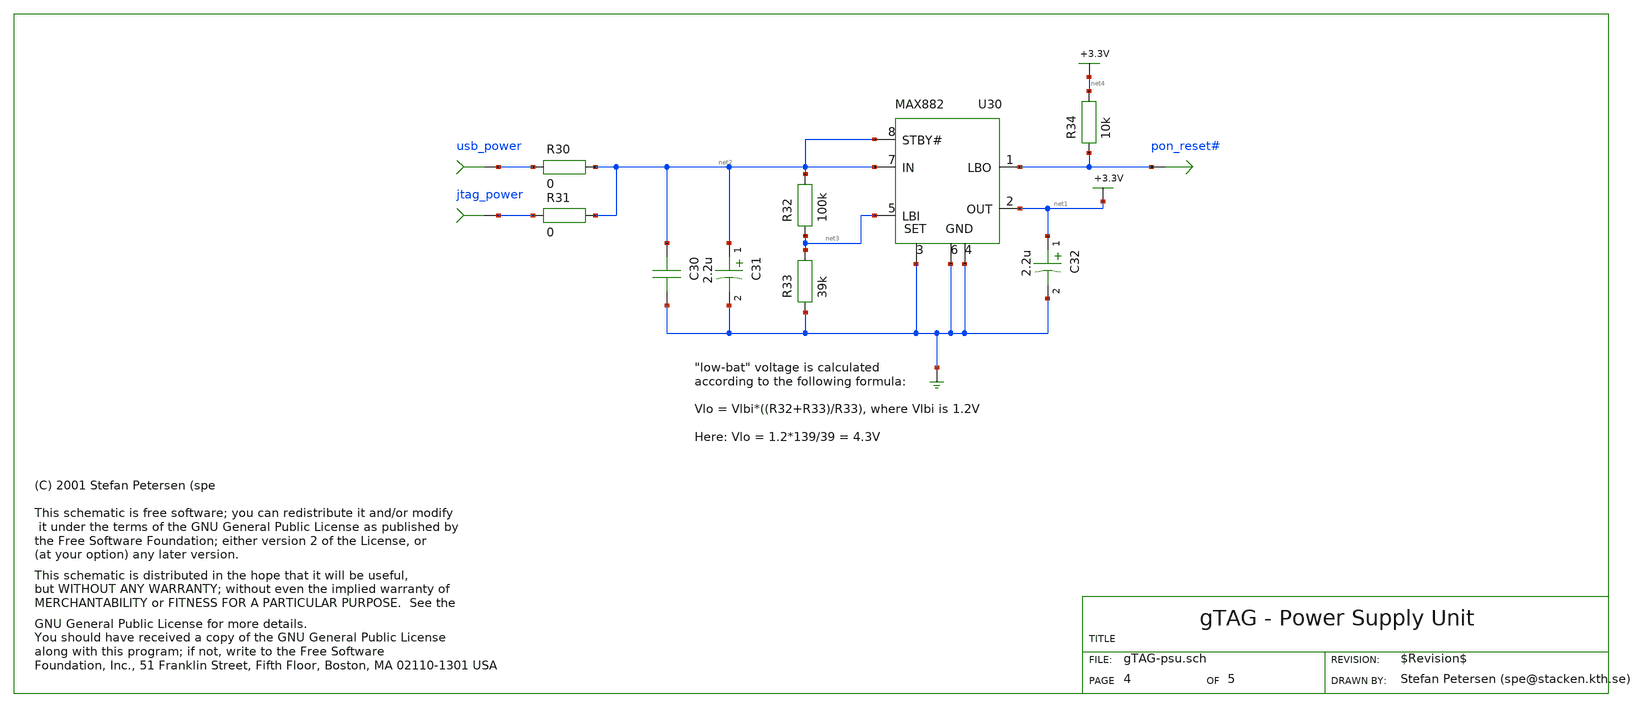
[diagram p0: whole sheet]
** sch_path: xschem_library/gschem_import/gTAG-psu.sch
* copyleft.sym
**.subckt gTAG-psu usb_power jtag_power pon_reset#
U30 net2 net2 net3 GND GND GND net1 pon_reset#
C32 net1 GND 2.2u
C31 net2 GND 2.2u
R30 usb_power net2 0
R31 jtag_power net2 0
C30 net2 GND 100n
R33 GND net3 39k
R32 net3 net2 100k
R34 pon_reset# net4 10k
**.ends
.end
